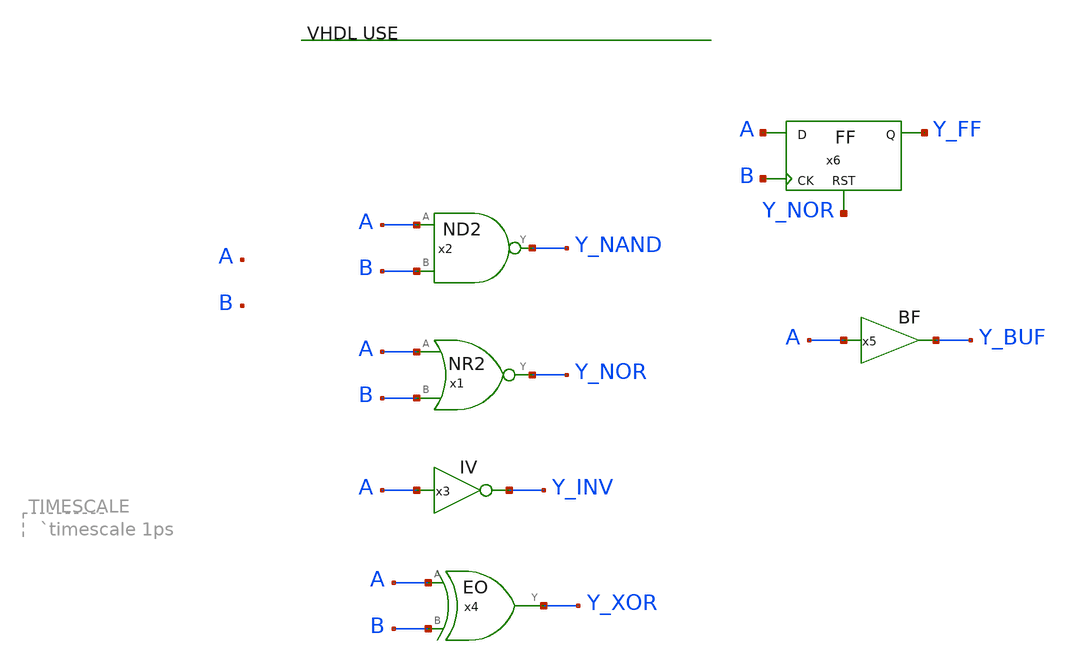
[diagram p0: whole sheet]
** sch_path: xschem_library/logic/testbench.sch
**.subckt testbench
x1 Y_NOR A B nr2
x2 [ A B ] Y_NAND nand
x3 Y_INV A iv
x4 Y_XOR A B eo
x5 Y_BUF A bf
x6 A Y_FF B Y_NOR ff
**.ends

* expanding   symbol:  logic/nr2.sym # of pins=3
** sym_path: xschem_library/logic/nr2.sym
** sch_path: xschem_library/logic/nr2.sch
.subckt nr2 Y A B  delay=200 ps del=200
*.opin Y
*.ipin A
*.ipin B
.ends


* expanding   symbol:  logic/nd2.sym # of pins=3
** sym_path: xschem_library/logic/nd2.sym
** sch_path: xschem_library/logic/nd2.sch
.subckt nd2 A B Y  delay=120 ps del=120
.ends


* expanding   symbol:  logic/iv.sym # of pins=2
** sym_path: xschem_library/logic/iv.sym
** sch_path: xschem_library/logic/iv.sch
.subckt iv Y A  delay=70 ps del=70
*.opin Y
*.ipin A
.ends


* expanding   symbol:  logic/eo.sym # of pins=3
** sym_path: xschem_library/logic/eo.sym
** sch_path: xschem_library/logic/eo.sch
.subckt eo Y A B  delay=220 ps del=220
*.ipin A
*.ipin B
*.opin Y
.ends


* expanding   symbol:  logic/bf.sym # of pins=2
** sym_path: xschem_library/logic/bf.sym
** sch_path: xschem_library/logic/bf.sch
.subckt bf Y A  delay=90 ps del=90
*.opin Y
*.ipin A
.ends


* expanding   symbol:  logic/ff.sym # of pins=4
** sym_path: xschem_library/logic/ff.sym
** sch_path: xschem_library/logic/ff.sch
.subckt ff D Q CK RST  delay=400 ps del=400
*.ipin D
*.opin Q
*.ipin CK
*.ipin RST
.ends

.end
